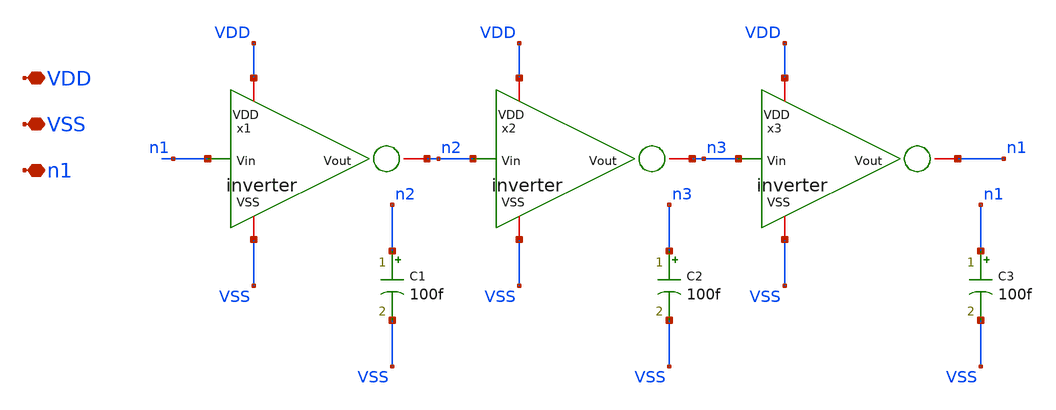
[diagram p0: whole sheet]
** sch_path: gf180_examples/inverter/xschem/3_stage_RO.sch
**.subckt 3_stage_RO VDD VSS n1
*.iopin VDD
*.iopin VSS
*.iopin n1
x1 n1 VDD VSS n2 inverter
x2 n2 VDD VSS n3 inverter
x3 n3 VDD VSS n1 inverter
C1 n2 VSS 100f m=1
C2 n3 VSS 100f m=1
C3 n1 VSS 100f m=1
**.ends
.end
